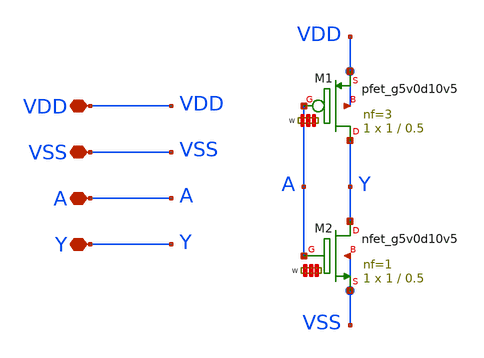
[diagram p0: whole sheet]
** sch_path: LIB/Sky130A/digital/inverter_5V.sch
**.subckt inverter_5V VDD VSS A Y
*.iopin VDD
*.iopin VSS
*.iopin A
*.iopin Y
XM1 Y A VDD VDD sky130_fd_pr__pfet_g5v0d10v5 L=0.5 W='1 * 3 ' nf=3 ad='int((3 + 1)/2) * 1 * 0.29' as='int((3 + 2)/2) * 1 * 0.29'
+ pd='2*int((3 + 1)/2) * (1 + 0.29)' ps='2*int((3 + 2)/2) * (1 + 0.29)' nrd='0.29 / 1 / 3 ' nrs='0.29 / 1 / 3 '
+ sa=0 sb=0 sd=0 mult=1 m=1
XM2 Y A VSS VSS sky130_fd_pr__nfet_g5v0d10v5 L=0.5 W='1 * 1 ' nf=1 ad='int((nf+1)/2) * W / nf * 0.29'
+ as='int((nf+2)/2) * W / nf * 0.29' pd='2*int((nf+1)/2) * (W / nf + 0.29)' ps='2*int((nf+2)/2) * (W / nf + 0.29)'
+ nrd='0.29 / W ' nrs='0.29 / W ' sa=0 sb=0 sd=0 mult=1 m=1
**.ends
.end
